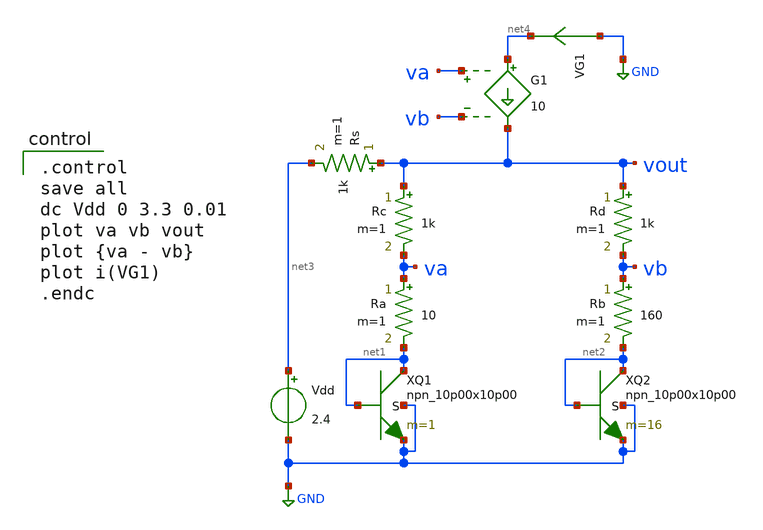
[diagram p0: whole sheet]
** sch_path: bgr/npn-diode-vccs.sch
**.subckt npn-diode-vccs
XQ1 net1 net1 GND GND npn_10p00x10p00 m=1
Vdd net3 GND 2.4
XQ2 net2 net2 GND GND npn_10p00x10p00 m=16
Rb vb net2 160 m=1
Ra va net1 10 m=1
Rc vout va 1k m=1
Rd vout vb 1k m=1
Rs vout net3 1k m=1
G1 net4 vout va vb 10
VG1 GND net4 0
.save i(vg1)
**** begin user architecture code

.include $::180MCU_MODELS/design.ngspice
.lib $::180MCU_MODELS/sm141064.ngspice typical
.lib $::180MCU_MODELS/sm141064.ngspice res_typical
.lib $::180MCU_MODELS/sm141064.ngspice moscap_typical
.lib $::180MCU_MODELS/sm141064.ngspice bjt_typical
* .lib $::180MCU_MODELS/sm141064.ngspice res_statistical


.control
save all
dc Vdd 0 3.3 0.01
plot va vb vout
plot {va - vb}
plot i(VG1)
.endc

**** end user architecture code
**.ends
.GLOBAL GND
.end
